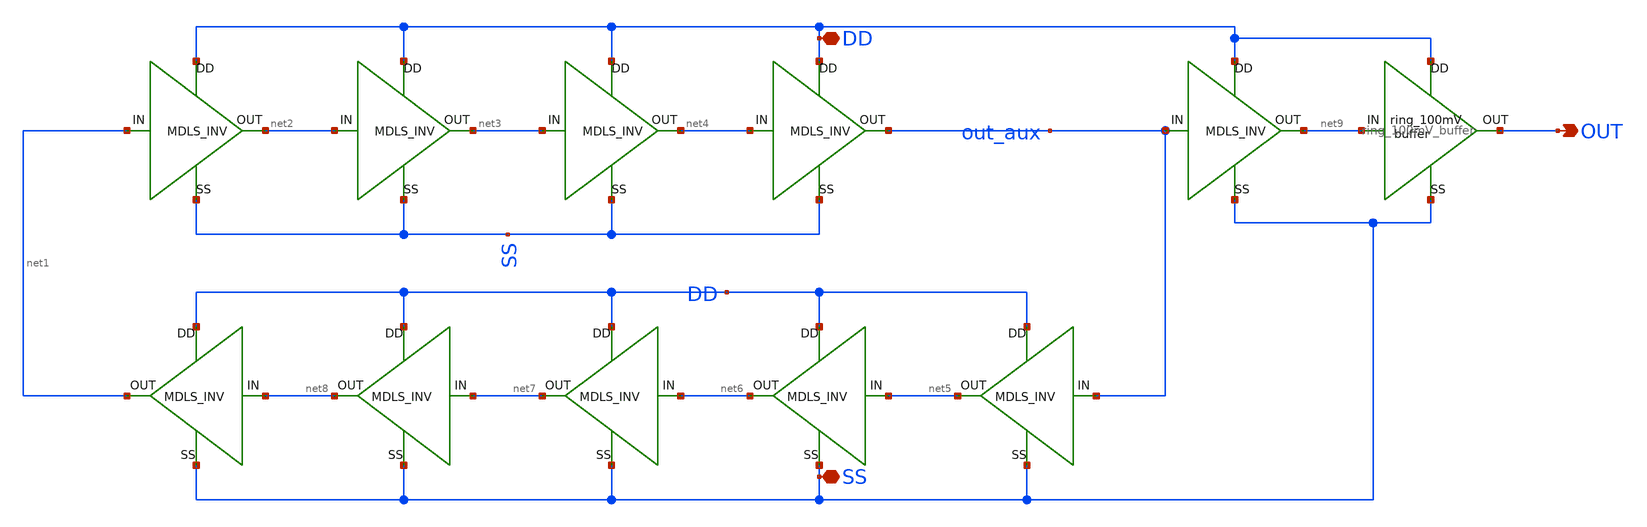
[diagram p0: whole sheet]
** sch_path: xschem/ring_100mV.sch
**.subckt ring_100mV DD SS OUT
*.iopin DD
*.iopin SS
*.opin OUT
X2 net1 net2 DD SS mdls_inv
X1 net2 net3 DD SS mdls_inv
X3 net3 net4 DD SS mdls_inv
X4 net4 out_aux DD SS mdls_inv
X10 out_aux net5 DD SS mdls_inv
X11 net5 net6 DD SS mdls_inv
X12 net6 net7 DD SS mdls_inv
X13 net7 net8 DD SS mdls_inv
X14 net8 net1 DD SS mdls_inv
X5 out_aux net9 DD SS mdls_inv
X6 net9 OUT DD SS ring_100mV_buffer
**.ends

* expanding   symbol:  mdls_inv.sym # of pins=4
** sym_path: xschem/mdls_inv.sym
** sch_path: xschem/mdls_inv.sch
.subckt mdls_inv IN OUT DD SS
*.ipin IN
*.iopin DD
*.iopin SS
*.opin OUT
XM5 OUT IN net1 SS sky130_fd_pr__nfet_01v8_lvt L=0.8 W=5.5 nf=1 ad='int((nf+1)/2) * W/nf * 0.29' as='int((nf+2)/2) * W/nf * 0.29'
+ pd='2*int((nf+1)/2) * (W/nf + 0.29)' ps='2*int((nf+2)/2) * (W/nf + 0.29)' nrd='0.29 / W' nrs='0.29 / W'
+ sa=0 sb=0 sd=0 mult=4 m=4
XM10 OUT IN net2 DD sky130_fd_pr__pfet_01v8_lvt L=0.8 W=1 nf=1 ad='int((nf+1)/2) * W/nf * 0.29' as='int((nf+2)/2) * W/nf * 0.29'
+ pd='2*int((nf+1)/2) * (W/nf + 0.29)' ps='2*int((nf+2)/2) * (W/nf + 0.29)' nrd='0.29 / W' nrs='0.29 / W'
+ sa=0 sb=0 sd=0 mult=1 m=1
XM11 net1 IN SS SS sky130_fd_pr__nfet_01v8_lvt L=1 W=5.5 nf=1 ad='int((nf+1)/2) * W/nf * 0.29' as='int((nf+2)/2) * W/nf * 0.29'
+ pd='2*int((nf+1)/2) * (W/nf + 0.29)' ps='2*int((nf+2)/2) * (W/nf + 0.29)' nrd='0.29 / W' nrs='0.29 / W'
+ sa=0 sb=0 sd=0 mult=2 m=2
XM13 net2 IN DD DD sky130_fd_pr__pfet_01v8_lvt L=2 W=1 nf=1 ad='int((nf+1)/2) * W/nf * 0.29' as='int((nf+2)/2) * W/nf * 0.29'
+ pd='2*int((nf+1)/2) * (W/nf + 0.29)' ps='2*int((nf+2)/2) * (W/nf + 0.29)' nrd='0.29 / W' nrs='0.29 / W'
+ sa=0 sb=0 sd=0 mult=1 m=1
XM1 net1 OUT SS DD sky130_fd_pr__pfet_01v8_lvt L=0.8 W=1 nf=1 ad='int((nf+1)/2) * W/nf * 0.29' as='int((nf+2)/2) * W/nf * 0.29'
+ pd='2*int((nf+1)/2) * (W/nf + 0.29)' ps='2*int((nf+2)/2) * (W/nf + 0.29)' nrd='0.29 / W' nrs='0.29 / W'
+ sa=0 sb=0 sd=0 mult=1 m=1
XM2 net2 OUT DD SS sky130_fd_pr__nfet_01v8_lvt L=0.4 W=5.5 nf=1 ad='int((nf+1)/2) * W/nf * 0.29' as='int((nf+2)/2) * W/nf * 0.29'
+ pd='2*int((nf+1)/2) * (W/nf + 0.29)' ps='2*int((nf+2)/2) * (W/nf + 0.29)' nrd='0.29 / W' nrs='0.29 / W'
+ sa=0 sb=0 sd=0 mult=2 m=2
.ends


* expanding   symbol:  ring_100mV_buffer.sym # of pins=4
** sym_path: xschem/ring_100mV_buffer.sym
** sch_path: xschem/ring_100mV_buffer.sch
.subckt ring_100mV_buffer IN OUT DD SS
*.opin OUT
*.iopin DD
*.iopin SS
*.ipin IN
XM5 net1 IN SS SS sky130_fd_pr__nfet_01v8_lvt L=0.8 W=5.5 nf=1 ad='int((nf+1)/2) * W/nf * 0.29' as='int((nf+2)/2) * W/nf * 0.29'
+ pd='2*int((nf+1)/2) * (W/nf + 0.29)' ps='2*int((nf+2)/2) * (W/nf + 0.29)' nrd='0.29 / W' nrs='0.29 / W'
+ sa=0 sb=0 sd=0 mult=8 m=8
XM10 net1 IN DD DD sky130_fd_pr__pfet_01v8_lvt L=0.8 W=1 nf=1 ad='int((nf+1)/2) * W/nf * 0.29' as='int((nf+2)/2) * W/nf * 0.29'
+ pd='2*int((nf+1)/2) * (W/nf + 0.29)' ps='2*int((nf+2)/2) * (W/nf + 0.29)' nrd='0.29 / W' nrs='0.29 / W'
+ sa=0 sb=0 sd=0 mult=2 m=2
XM1 OUT net1 SS SS sky130_fd_pr__nfet_01v8_lvt L=0.8 W=5.5 nf=1 ad='int((nf+1)/2) * W/nf * 0.29' as='int((nf+2)/2) * W/nf * 0.29'
+ pd='2*int((nf+1)/2) * (W/nf + 0.29)' ps='2*int((nf+2)/2) * (W/nf + 0.29)' nrd='0.29 / W' nrs='0.29 / W'
+ sa=0 sb=0 sd=0 mult=16 m=16
XM2 OUT net1 DD DD sky130_fd_pr__pfet_01v8_lvt L=0.8 W=1 nf=1 ad='int((nf+1)/2) * W/nf * 0.29' as='int((nf+2)/2) * W/nf * 0.29'
+ pd='2*int((nf+1)/2) * (W/nf + 0.29)' ps='2*int((nf+2)/2) * (W/nf + 0.29)' nrd='0.29 / W' nrs='0.29 / W'
+ sa=0 sb=0 sd=0 mult=4 m=4
.ends

.end
